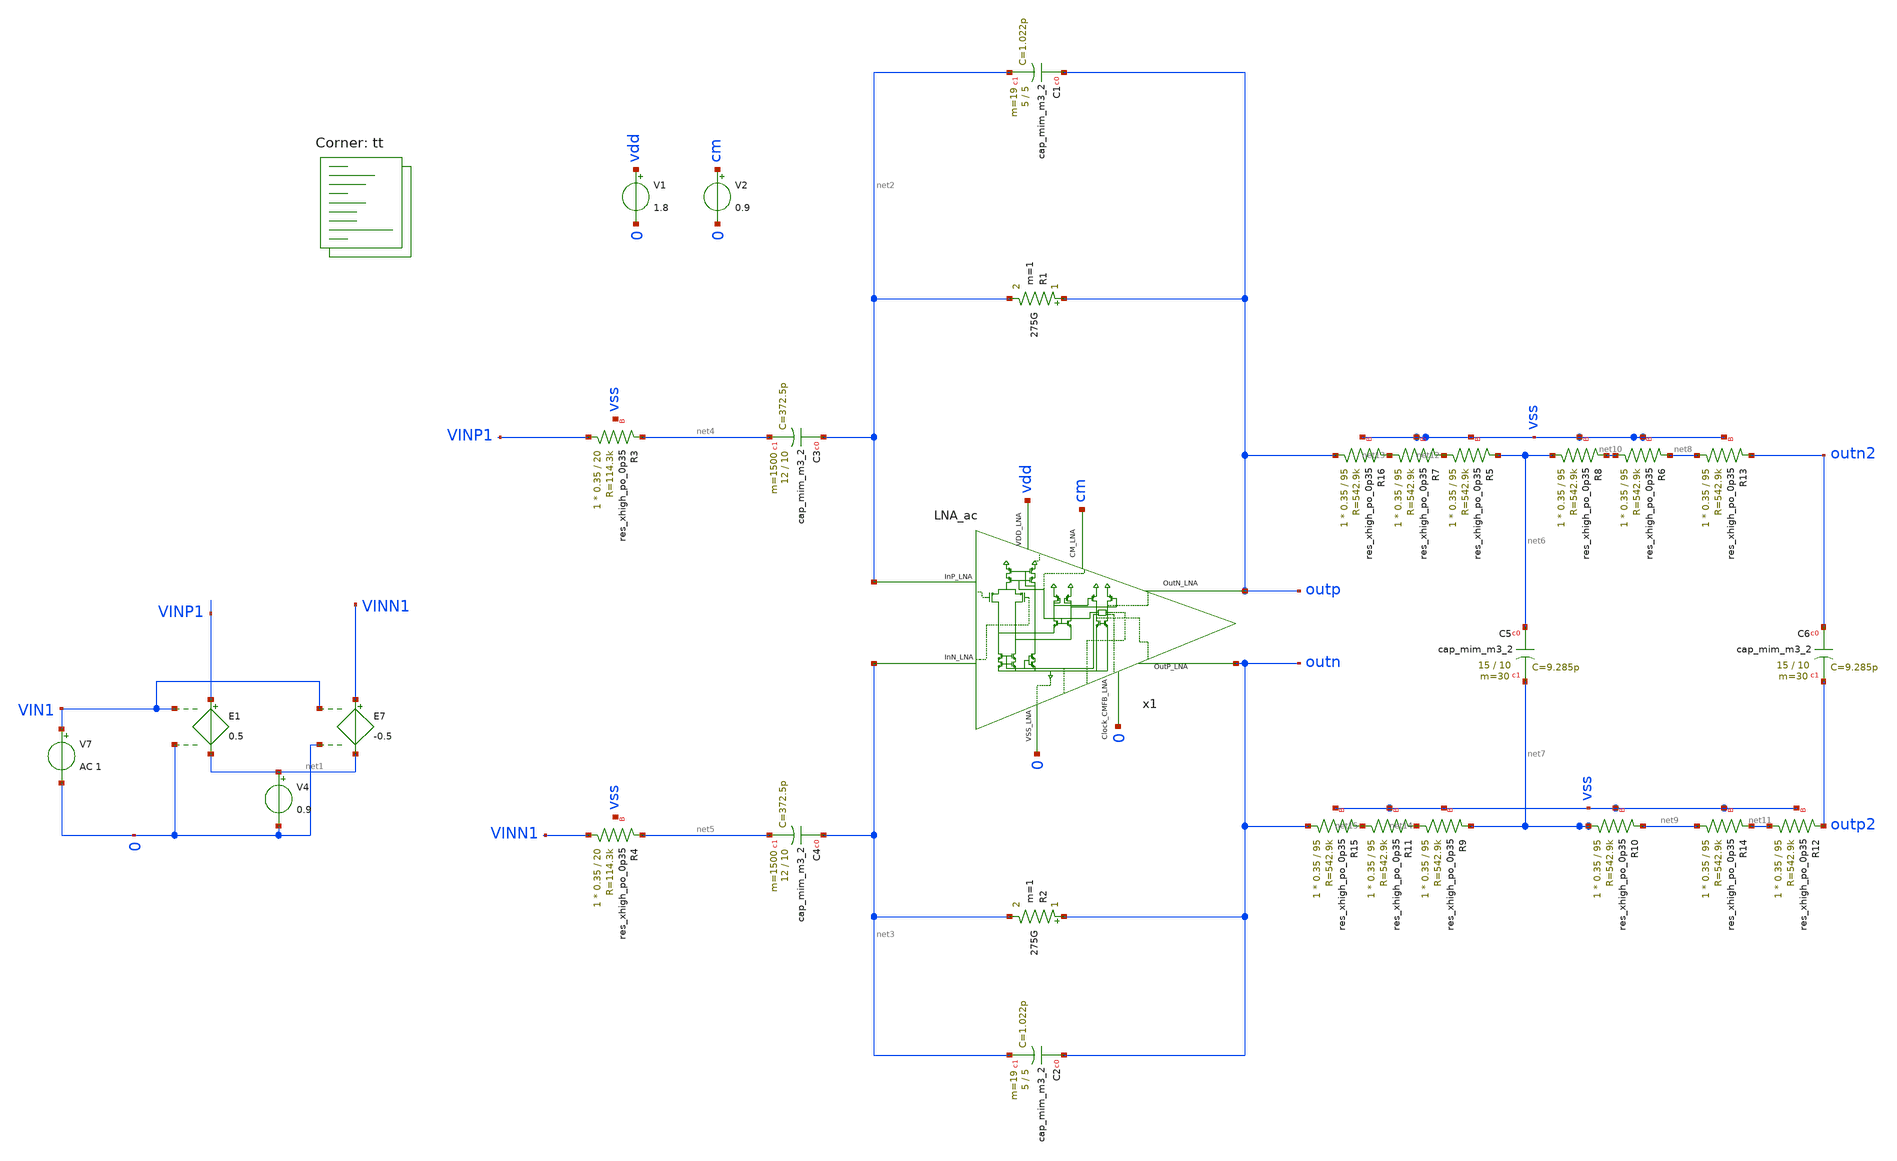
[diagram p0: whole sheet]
** sch_path: CL_ac.sch
**.subckt CL_ac
x1 net3 net2 vdd cm outp outn 0 0 LNA_ac
V1 vdd 0 1.8
V2 cm 0 0.9
E1 VINP1 net1 VIN1 0 0.5
E7 VINN1 net1 VIN1 0 -0.5
V4 net1 0 0.9
V7 VIN1 0 AC 1
R1 outp net2 275G m=1
XC1 outp net2 sky130_fd_pr__cap_mim_m3_2 W=5 L=5 MF=19 m=19
XC2 outn net3 sky130_fd_pr__cap_mim_m3_2 W=5 L=5 MF=19 m=19
R2 outn net3 275G m=1
XC3 net2 net4 sky130_fd_pr__cap_mim_m3_2 W=12 L=10 MF=1500 m=1500
XC4 net3 net5 sky130_fd_pr__cap_mim_m3_2 W=12 L=10 MF=1500 m=1500
XR3 VINP1 net4 vss sky130_fd_pr__res_xhigh_po_0p35 L=20 mult=1 m=1
XR4 VINN1 net5 vss sky130_fd_pr__res_xhigh_po_0p35 L=20 mult=1 m=1
XC5 net6 net7 sky130_fd_pr__cap_mim_m3_2 W=15 L=10 MF=30 m=30
XC6 outn2 outp2 sky130_fd_pr__cap_mim_m3_2 W=15 L=10 MF=30 m=30
XR5 net12 net6 vss sky130_fd_pr__res_xhigh_po_0p35 L=95 mult=1 m=1
XR6 net10 net8 vss sky130_fd_pr__res_xhigh_po_0p35 L=95 mult=1 m=1
XR7 net13 net12 vss sky130_fd_pr__res_xhigh_po_0p35 L=95 mult=1 m=1
XR8 net6 net10 vss sky130_fd_pr__res_xhigh_po_0p35 L=95 mult=1 m=1
XR9 net14 net7 vss sky130_fd_pr__res_xhigh_po_0p35 L=95 mult=1 m=1
XR10 net7 net9 vss sky130_fd_pr__res_xhigh_po_0p35 L=95 mult=1 m=1
XR11 net15 net14 vss sky130_fd_pr__res_xhigh_po_0p35 L=95 mult=1 m=1
XR14 net9 net11 vss sky130_fd_pr__res_xhigh_po_0p35 L=95 mult=1 m=1
XR12 net11 outp2 vss sky130_fd_pr__res_xhigh_po_0p35 L=95 mult=1 m=1
XR13 net8 outn2 vss sky130_fd_pr__res_xhigh_po_0p35 L=95 mult=1 m=1
XR15 outn net15 vss sky130_fd_pr__res_xhigh_po_0p35 L=95 mult=1 m=1
XR16 outp net13 vss sky130_fd_pr__res_xhigh_po_0p35 L=95 mult=1 m=1
**** begin user architecture code
.lib $::SKYWATER_MODELS/sky130.lib.spice tt


.options savecurrents
.options gmin=1e-13
*ic v(VM5)=0.9 v(VM6)=0.9
.control

save all


*nmos
save @m.xm11.msky130_fd_pr__nfet_01v8_lvt[vgs]
save @m.xm4.msky130_fd_pr__nfet_01v8_lvt[vth]
save @m.xm4.msky130_fd_pr__nfet_01v8_lvt[vds]


save @m.xm5.msky130_fd_pr__nfet_01v8_lvt[vgs]
save @m.xm5.msky130_fd_pr__nfet_01v8_lvt[vth]
save @m.xm5.msky130_fd_pr__nfet_01v8_lvt[vds]

save @m.xm8.msky130_fd_pr__nfet_01v8_lvt[vgs]
save @m.xm8.msky130_fd_pr__nfet_01v8_lvt[vth]
save @m.xm8.msky130_fd_pr__nfet_01v8_lvt[vds]

save @m.xm9.msky130_fd_pr__nfet_01v8_lvt[vgs]
save @m.xm9.msky130_fd_pr__nfet_01v8_lvt[vth]
save @m.xm9.msky130_fd_pr__nfet_01v8_lvt[vds]

save @m.xm7.msky130_fd_pr__nfet_01v8_lvt[vgs]
save @m.xm7.msky130_fd_pr__nfet_01v8_lvt[vth]
save @m.xm7.msky130_fd_pr__nfet_01v8_lvt[vds]

save @m.xm11.msky130_fd_pr__nfet_01v8_lvt[vgs]
save @m.xm11.msky130_fd_pr__nfet_01v8_lvt[vth]
save @m.xm11.msky130_fd_pr__nfet_01v8_lvt[vds]


save @m.xm12.msky130_fd_pr__nfet_01v8_lvt[vgs]
save @m.xm12.msky130_fd_pr__nfet_01v8_lvt[vth]
save @m.xm12.msky130_fd_pr__nfet_01v8_lvt[vds]


save @m.xm13.msky130_fd_pr__nfet_01v8_lvt[vgs]
save @m.xm13.msky130_fd_pr__nfet_01v8_lvt[vth]
save @m.xm13.msky130_fd_pr__nfet_01v8_lvt[vds]


save @m.xm10.msky130_fd_pr__nfet_01v8_lvt[vgs]
save @m.xm10.msky130_fd_pr__nfet_01v8_lvt[vth]
save @m.xm10.msky130_fd_pr__nfet_01v8_lvt[vds]


save @m.xm11.msky130_fd_pr__nfet_01v8_lvt[vgs]
save @m.xm11.msky130_fd_pr__nfet_01v8_lvt[vth]
save @m.xm11.msky130_fd_pr__nfet_01v8_lvt[vds]


save @m.xm12.msky130_fd_pr__nfet_01v8_lvt[vgs]
save @m.xm12.msky130_fd_pr__nfet_01v8_lvt[vth]
save @m.xm12.msky130_fd_pr__nfet_01v8_lvt[vds]


save @m.xm13.msky130_fd_pr__nfet_01v8_lvt[vgs]
save @m.xm13.msky130_fd_pr__nfet_01v8_lvt[vth]
save @m.xm13.msky130_fd_pr__nfet_01v8_lvt[vds]




*pmos

save @m.xm2.msky130_fd_pr__pfet_01v8_lvt[vgs]
save @m.xm2.msky130_fd_pr__pfet_01v8_lvt[vth]
save @m.xm2.msky130_fd_pr__pfet_01v8_lvt[vds]


save @m.xm3.msky130_fd_pr__pfet_01v8_lvt[vgs]
save @m.xm3.msky130_fd_pr__pfet_01v8_lvt[vth]
save @m.xm3.msky130_fd_pr__pfet_01v8_lvt[vds]
save @m.xm3.msky130_fd_pr__pfet_01v8_lvt[gds]


save @m.xm10.msky130_fd_pr__pfet_01v8_lvt[vgs]
save @m.xm10.msky130_fd_pr__pfet_01v8_lvt[vth]
save @m.xm10.msky130_fd_pr__pfet_01v8_lvt[vds]


save @m.xm23.msky130_fd_pr__pfet_01v8_lvt[vgs]
save @m.xm23.msky130_fd_pr__pfet_01v8_lvt[vth]
save @m.xm23.msky130_fd_pr__pfet_01v8_lvt[vds]


save @m.xm24.msky130_fd_pr__pfet_01v8_lvt[vgs]
save @m.xm24.msky130_fd_pr__pfet_01v8_lvt[vth]
save @m.xm24.msky130_fd_pr__pfet_01v8_lvt[vds]
save @m.xm24.msky130_fd_pr__pfet_01v8_lvt[gds]


op
remzerovec
write CL_ac.raw
*set appendwrite


.endc
.control



*tran 50u 1500m
*save all
*plot v(Outp)-v(outn)


noise V(Outp,Outn) V7 dec 100 0.1 128
print inoise_total onoise_total
setplot noise1
plot inoise_spectrum

ac dec 10 0.1 20k
let gaind=(v(outp2)-v(outn2))/(v(VINP1)-v(VINN1))
plot db(gaind)


.endc






.include $::SKYWATER_STDCELLS/sky130_fd_sc_hd.spice

**** end user architecture code
**.ends

* expanding   symbol:  LNA/LNA_ac.sym # of pins=8
** sym_path: LNA_ac.sym
** sch_path: LNA_ac.sch
.subckt LNA_ac InN_LNA InP_LNA VDD_LNA CM_LNA OutN_LNA OutP_LNA Clock_CMFB_LNA VSS_LNA
*.iopin InP_LNA
*.iopin InN_LNA
*.iopin VSS_LNA
*.iopin VDD_LNA
*.iopin CM_LNA
*.iopin OutP_LNA
*.iopin OutN_LNA
*.iopin Clock_CMFB_LNA
XM7 net1 InP_LNA VT2 VT2 sky130_fd_pr__pfet_01v8_lvt L=10 W=90 nf=1 ad='int((nf+1)/2) * W/nf * 0.29'
+ as='int((nf+2)/2) * W/nf * 0.29' pd='2*int((nf+1)/2) * (W/nf + 0.29)' ps='2*int((nf+2)/2) * (W/nf + 0.29)'
+ nrd='0.29 / W' nrs='0.29 / W' sa=0 sb=0 sd=0 mult=5 m=5
XM10 net2 InN_LNA VT2 VT2 sky130_fd_pr__pfet_01v8_lvt L=10 W=90 nf=1 ad='int((nf+1)/2) * W/nf * 0.29'
+ as='int((nf+2)/2) * W/nf * 0.29' pd='2*int((nf+1)/2) * (W/nf + 0.29)' ps='2*int((nf+2)/2) * (W/nf + 0.29)'
+ nrd='0.29 / W' nrs='0.29 / W' sa=0 sb=0 sd=0 mult=5 m=5
XM11 net1 vbias VSS_LNA VSS_LNA sky130_fd_pr__nfet_01v8_lvt L=20 W=10 nf=1 ad='int((nf+1)/2) * W/nf * 0.29'
+ as='int((nf+2)/2) * W/nf * 0.29' pd='2*int((nf+1)/2) * (W/nf + 0.29)' ps='2*int((nf+2)/2) * (W/nf + 0.29)'
+ nrd='0.29 / W' nrs='0.29 / W' sa=0 sb=0 sd=0 mult=4 m=4
XM12 net2 vbias VSS_LNA VSS_LNA sky130_fd_pr__nfet_01v8_lvt L=20 W=10 nf=1 ad='int((nf+1)/2) * W/nf * 0.29'
+ as='int((nf+2)/2) * W/nf * 0.29' pd='2*int((nf+1)/2) * (W/nf + 0.29)' ps='2*int((nf+2)/2) * (W/nf + 0.29)'
+ nrd='0.29 / W' nrs='0.29 / W' sa=0 sb=0 sd=0 mult=4 m=4
XM13 drain_m18 drain_m18 VDD_LNA VDD_LNA sky130_fd_pr__pfet_01v8_lvt L=20 W=6 nf=1 ad='int((nf+1)/2) * W/nf * 0.29'
+ as='int((nf+2)/2) * W/nf * 0.29' pd='2*int((nf+1)/2) * (W/nf + 0.29)' ps='2*int((nf+2)/2) * (W/nf + 0.29)'
+ nrd='0.29 / W' nrs='0.29 / W' sa=0 sb=0 sd=0 mult=1 m=1
XM14 drain_m19 drain_m19 VDD_LNA VDD_LNA sky130_fd_pr__pfet_01v8_lvt L=20 W=6 nf=1 ad='int((nf+1)/2) * W/nf * 0.29'
+ as='int((nf+2)/2) * W/nf * 0.29' pd='2*int((nf+1)/2) * (W/nf + 0.29)' ps='2*int((nf+2)/2) * (W/nf + 0.29)'
+ nrd='0.29 / W' nrs='0.29 / W' sa=0 sb=0 sd=0 mult=1 m=1
XM15 drain_m18 CM_LNA net2 VSS_LNA sky130_fd_pr__nfet_01v8_lvt L=20 W=1 nf=1 ad='int((nf+1)/2) * W/nf * 0.29'
+ as='int((nf+2)/2) * W/nf * 0.29' pd='2*int((nf+1)/2) * (W/nf + 0.29)' ps='2*int((nf+2)/2) * (W/nf + 0.29)'
+ nrd='0.29 / W' nrs='0.29 / W' sa=0 sb=0 sd=0 mult=1 m=1
XM22 drain_m19 CM_LNA net1 VSS_LNA sky130_fd_pr__nfet_01v8_lvt L=20 W=1 nf=1 ad='int((nf+1)/2) * W/nf * 0.29'
+ as='int((nf+2)/2) * W/nf * 0.29' pd='2*int((nf+1)/2) * (W/nf + 0.29)' ps='2*int((nf+2)/2) * (W/nf + 0.29)'
+ nrd='0.29 / W' nrs='0.29 / W' sa=0 sb=0 sd=0 mult=1 m=1
XM24 OutP_LNA drain_m19 VDD_LNA VDD_LNA sky130_fd_pr__pfet_01v8_lvt L=20 W=6 nf=1 ad='int((nf+1)/2) * W/nf * 0.29'
+ as='int((nf+2)/2) * W/nf * 0.29' pd='2*int((nf+1)/2) * (W/nf + 0.29)' ps='2*int((nf+2)/2) * (W/nf + 0.29)'
+ nrd='0.29 / W' nrs='0.29 / W' sa=0 sb=0 sd=0 mult=10 m=10
XM26 OutN_LNA drain_m18 VDD_LNA VDD_LNA sky130_fd_pr__pfet_01v8_lvt L=20 W=6 nf=1 ad='int((nf+1)/2) * W/nf * 0.29'
+ as='int((nf+2)/2) * W/nf * 0.29' pd='2*int((nf+1)/2) * (W/nf + 0.29)' ps='2*int((nf+2)/2) * (W/nf + 0.29)'
+ nrd='0.29 / W' nrs='0.29 / W' sa=0 sb=0 sd=0 mult=10 m=10
XM27 OutN_LNA net4 VSS_LNA VSS_LNA sky130_fd_pr__nfet_01v8_lvt L=20 W=10 nf=1 ad='int((nf+1)/2) * W/nf * 0.29'
+ as='int((nf+2)/2) * W/nf * 0.29' pd='2*int((nf+1)/2) * (W/nf + 0.29)' ps='2*int((nf+2)/2) * (W/nf + 0.29)'
+ nrd='0.29 / W' nrs='0.29 / W' sa=0 sb=0 sd=0 mult=10 m=10
XM28 OutP_LNA net4 VSS_LNA VSS_LNA sky130_fd_pr__nfet_01v8_lvt L=20 W=10 nf=1 ad='int((nf+1)/2) * W/nf * 0.29'
+ as='int((nf+2)/2) * W/nf * 0.29' pd='2*int((nf+1)/2) * (W/nf + 0.29)' ps='2*int((nf+2)/2) * (W/nf + 0.29)'
+ nrd='0.29 / W' nrs='0.29 / W' sa=0 sb=0 sd=0 mult=10 m=10
XM29 VT2 net3 VDD_LNA VDD_LNA sky130_fd_pr__pfet_01v8_lvt L=20 W=2 nf=1 ad='int((nf+1)/2) * W/nf * 0.29'
+ as='int((nf+2)/2) * W/nf * 0.29' pd='2*int((nf+1)/2) * (W/nf + 0.29)' ps='2*int((nf+2)/2) * (W/nf + 0.29)'
+ nrd='0.29 / W' nrs='0.29 / W' sa=0 sb=0 sd=0 mult=6 m=6
XM30 net3 net3 VDD_LNA VDD_LNA sky130_fd_pr__pfet_01v8_lvt L=20 W=2 nf=1 ad='int((nf+1)/2) * W/nf * 0.29'
+ as='int((nf+2)/2) * W/nf * 0.29' pd='2*int((nf+1)/2) * (W/nf + 0.29)' ps='2*int((nf+2)/2) * (W/nf + 0.29)'
+ nrd='0.29 / W' nrs='0.29 / W' sa=0 sb=0 sd=0 mult=1 m=1
XM31 net3 vbias VSS_LNA VSS_LNA sky130_fd_pr__nfet_01v8_lvt L=20 W=10 nf=1 ad='int((nf+1)/2) * W/nf * 0.29'
+ as='int((nf+2)/2) * W/nf * 0.29' pd='2*int((nf+1)/2) * (W/nf + 0.29)' ps='2*int((nf+2)/2) * (W/nf + 0.29)'
+ nrd='0.29 / W' nrs='0.29 / W' sa=0 sb=0 sd=0 mult=1 m=1
E1 f1 VSS_LNA OutN_LNA VSS_LNA -1
E2 f2 VSS_LNA OutP_LNA f1 1
E7 f3 VSS_LNA f2 VSS_LNA 0.5
E8 net4 VSS_LNA CM_LNA f3 {-500}
XM1 vbias vbias VSS_LNA VSS_LNA sky130_fd_pr__nfet_01v8_lvt L=20 W=10 nf=1 ad='int((nf+1)/2) * W/nf * 0.29'
+ as='int((nf+2)/2) * W/nf * 0.29' pd='2*int((nf+1)/2) * (W/nf + 0.29)' ps='2*int((nf+2)/2) * (W/nf + 0.29)'
+ nrd='0.29 / W' nrs='0.29 / W' sa=0 sb=0 sd=0 mult=1 m=1
I0 VDD_LNA vbias 50n
.ends

.end
